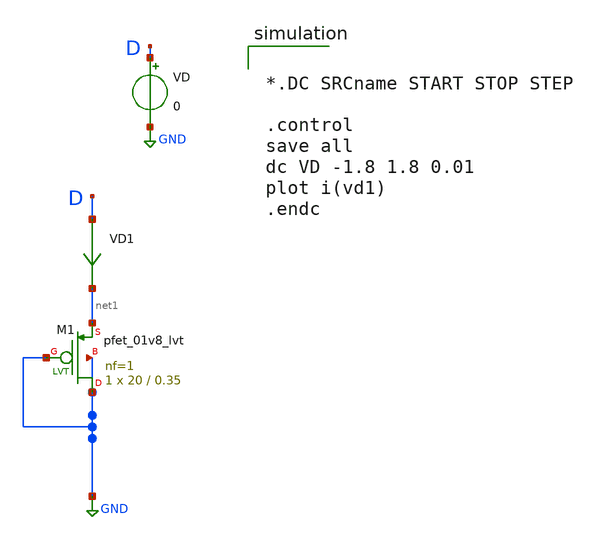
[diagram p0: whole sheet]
** sch_path: xschem/diodo-I-V-pnp.sch
**.subckt diodo-I-V-pnp
XM1 GND GND net1 GND sky130_fd_pr__pfet_01v8_lvt L=0.35 W=20 nf=1 ad='int((1 + 1)/2) * 20 / 1 * 0.29'
+ as='int((1 + 2)/2) * 20 / 1 * 0.29' pd='2*int((1 + 1)/2) * (20 / 1 + 0.29)' ps='2*int((1 + 2)/2) * (20 / 1 + 0.29)'
+ nrd='0.29 / 20 ' nrs='0.29 / 20 ' sa=0 sb=0 sd=0 mult=1 m=1
VD D GND 0
VD1 D net1 0
.save i(vd1)
**** begin user architecture code

** opencircuitdesign pdks install
.lib $::SKYWATER_MODELS/sky130.lib.spice tt




*.DC SRCname START STOP STEP

.control
save all
dc VD -1.8 1.8 0.01
plot i(vd1)
.endc



**** end user architecture code
**.ends
.GLOBAL GND
.end
